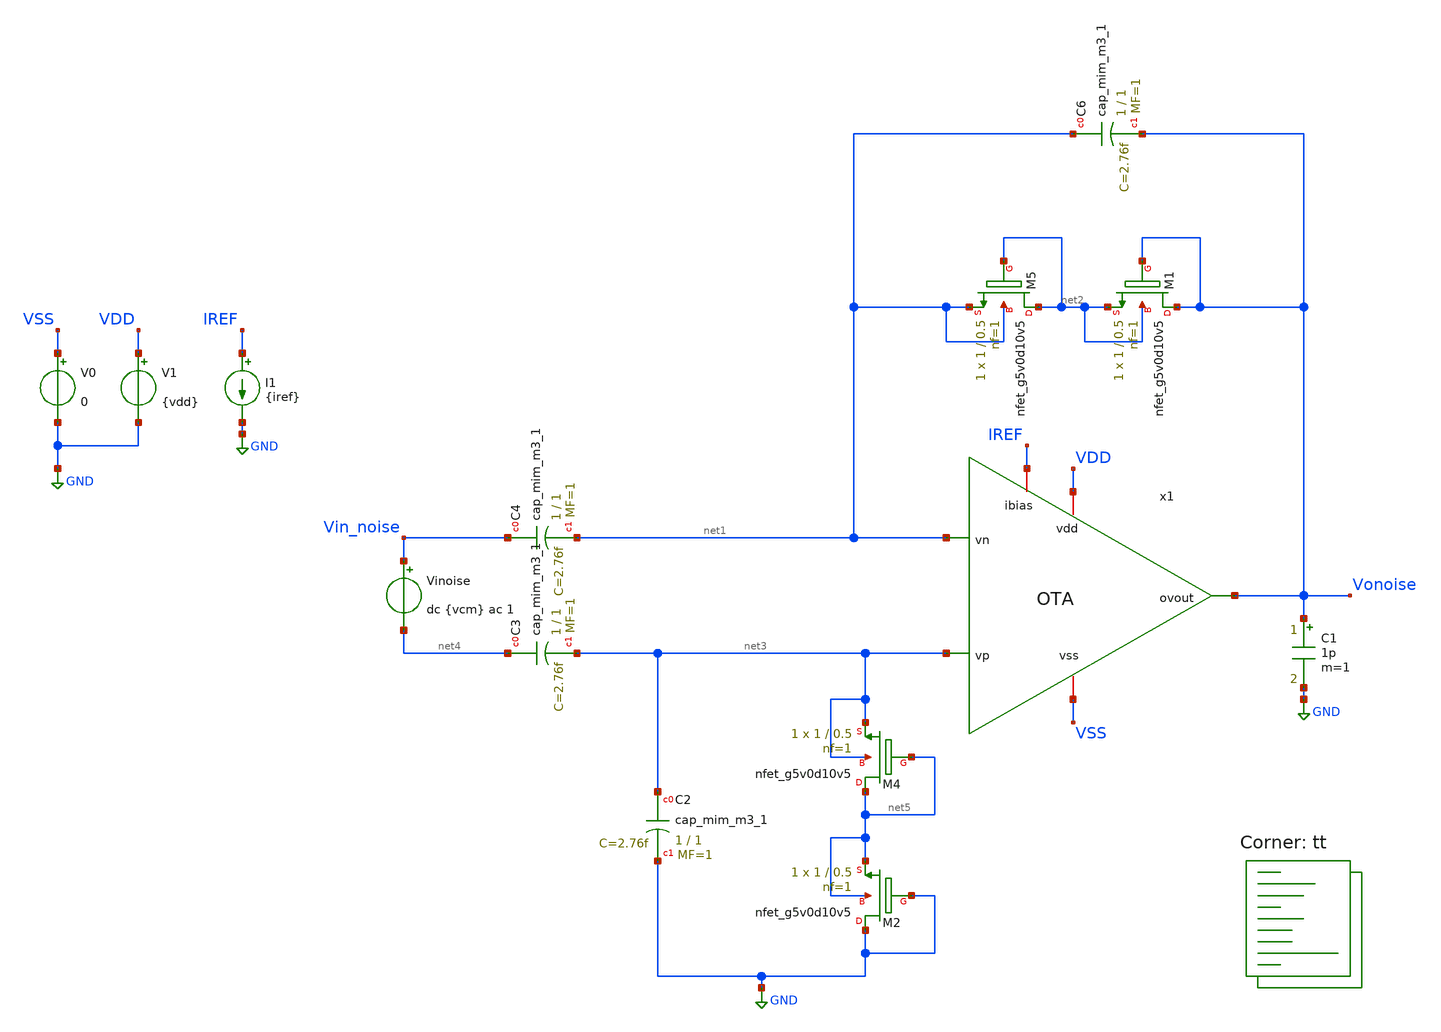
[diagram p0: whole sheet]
** sch_path: xschem/LNA_tb_noise.sch
**.subckt LNA_tb_noise
V0 VSS GND 0
V1 VDD GND {vdd}
C1 Vonoise GND 1p m=1
XC6 net1 Vonoise sky130_fd_pr__cap_mim_m3_1 W=1 L=1 MF=1 m=1
XC2 net3 GND sky130_fd_pr__cap_mim_m3_1 W=1 L=1 MF=1 m=1
XC3 net4 net3 sky130_fd_pr__cap_mim_m3_1 W=1 L=1 MF=1 m=1
XC4 Vin_noise net1 sky130_fd_pr__cap_mim_m3_1 W=1 L=1 MF=1 m=1
XM5 net2 net2 net1 net1 sky130_fd_pr__nfet_g5v0d10v5 L=0.5 W=1 nf=1 ad='int((nf+1)/2) * W/nf * 0.29'
+ as='int((nf+2)/2) * W/nf * 0.29' pd='2*int((nf+1)/2) * (W/nf + 0.29)' ps='2*int((nf+2)/2) * (W/nf + 0.29)'
+ nrd='0.29 / W' nrs='0.29 / W' sa=0 sb=0 sd=0 mult=1 m=1
XM1 Vonoise Vonoise net2 net2 sky130_fd_pr__nfet_g5v0d10v5 L=0.5 W=1 nf=1 ad='int((nf+1)/2) * W/nf * 0.29'
+ as='int((nf+2)/2) * W/nf * 0.29' pd='2*int((nf+1)/2) * (W/nf + 0.29)' ps='2*int((nf+2)/2) * (W/nf + 0.29)'
+ nrd='0.29 / W' nrs='0.29 / W' sa=0 sb=0 sd=0 mult=1 m=1
XM4 net5 net5 net3 net3 sky130_fd_pr__nfet_g5v0d10v5 L=0.5 W=1 nf=1 ad='int((nf+1)/2) * W/nf * 0.29'
+ as='int((nf+2)/2) * W/nf * 0.29' pd='2*int((nf+1)/2) * (W/nf + 0.29)' ps='2*int((nf+2)/2) * (W/nf + 0.29)'
+ nrd='0.29 / W' nrs='0.29 / W' sa=0 sb=0 sd=0 mult=1 m=1
XM2 GND GND net5 net5 sky130_fd_pr__nfet_g5v0d10v5 L=0.5 W=1 nf=1 ad='int((nf+1)/2) * W/nf * 0.29' as='int((nf+2)/2) * W/nf * 0.29'
+ pd='2*int((nf+1)/2) * (W/nf + 0.29)' ps='2*int((nf+2)/2) * (W/nf + 0.29)' nrd='0.29 / W' nrs='0.29 / W'
+ sa=0 sb=0 sd=0 mult=1 m=1
Vinoise Vin_noise net4 dc {vcm} ac 1
I1 IREF GND {iref}
x1 Vonoise VDD VSS IREF net1 net3 OTA
**** begin user architecture code

.param vdd=5
.param vcm=2.5
.param iref = 1u

.control
	save all
	save @m.x1.xm1a.msky130_fd_pr__pfet_g5v0d10v5[id] @m.x1.xm1a.msky130_fd_pr__pfet_g5v0d10v5[gm]
+ @m.x1.xm1a.msky130_fd_pr__pfet_g5v0d10v5[gds]
	save @m.x1.xm1b.msky130_fd_pr__pfet_g5v0d10v5[id] @m.x1.xm1b.msky130_fd_pr__pfet_g5v0d10v5[gm]
+ @m.x1.xm1b.msky130_fd_pr__pfet_g5v0d10v5[gds]
	save @m.x1.xm2a.msky130_fd_pr__pfet_g5v0d10v5[id] @m.x1.xm2a.msky130_fd_pr__pfet_g5v0d10v5[gm]
+ @m.x1.xm2a.msky130_fd_pr__pfet_g5v0d10v5[gds]
	save @m.x1.xm2b.msky130_fd_pr__pfet_g5v0d10v5[id] @m.x1.xm2b.msky130_fd_pr__pfet_g5v0d10v5[gm]
+ @m.x1.xm2b.msky130_fd_pr__pfet_g5v0d10v5[gds]
	save @m.x1.xm3a.msky130_fd_pr__nfet_g5v0d10v5[id] @m.x1.xm3a.msky130_fd_pr__nfet_g5v0d10v5[gm]
+ @m.x1.xm3a.msky130_fd_pr__nfet_g5v0d10v5[gds]
	save @m.x1.xm3b.msky130_fd_pr__nfet_g5v0d10v5[id] @m.x1.xm3b.msky130_fd_pr__nfet_g5v0d10v5[gm]
+ @m.x1.xm3b.msky130_fd_pr__nfet_g5v0d10v5[gds]
	save @m.x1.xm4a.msky130_fd_pr__nfet_g5v0d10v5[id] @m.x1.xm4a.msky130_fd_pr__nfet_g5v0d10v5[gm]
+ @m.x1.xm4a.msky130_fd_pr__nfet_g5v0d10v5[gds]
	save @m.x1.xm4b.msky130_fd_pr__nfet_g5v0d10v5[id] @m.x1.xm4b.msky130_fd_pr__nfet_g5v0d10v5[gm]
+ @m.x1.xm4b.msky130_fd_pr__nfet_g5v0d10v5[gds]
	save @m.x1.xm4c.msky130_fd_pr__nfet_g5v0d10v5[id] @m.x1.xm4c.msky130_fd_pr__nfet_g5v0d10v5[gm]
+ @m.x1.xm4c.msky130_fd_pr__nfet_g5v0d10v5[gds]
	save @m.x1.xm4d.msky130_fd_pr__nfet_g5v0d10v5[id] @m.x1.xm4d.msky130_fd_pr__nfet_g5v0d10v5[gm]
+ @m.x1.xm4d.msky130_fd_pr__nfet_g5v0d10v5[gds]
	save @m.x1.xm5a.msky130_fd_pr__pfet_g5v0d10v5[id] @m.x1.xm5a.msky130_fd_pr__pfet_g5v0d10v5[gm]
+ @m.x1.xm5a.msky130_fd_pr__pfet_g5v0d10v5[gds]
	save @m.x1.xm5b.msky130_fd_pr__pfet_g5v0d10v5[id] @m.x1.xm5b.msky130_fd_pr__pfet_g5v0d10v5[gm]
+ @m.x1.xm5b.msky130_fd_pr__pfet_g5v0d10v5[gds]
	save @m.x1.xm6.msky130_fd_pr__pfet_g5v0d10v5[id] @m.x1.xm6.msky130_fd_pr__pfet_g5v0d10v5[gm]
+ @m.x1.xm6.msky130_fd_pr__pfet_g5v0d10v5[gds]
	save @m.x1.xm7.msky130_fd_pr__pfet_g5v0d10v5[id] @m.x1.xm7.msky130_fd_pr__pfet_g5v0d10v5[gm]
+ @m.x1.xm7.msky130_fd_pr__pfet_g5v0d10v5[gds]

	op
	show

	noise v(Vonoise) Vinoise dec 20 1k 10e9
	setplot noise1
	write LNA_tb_noise1.raw noise1.all
	setplot noise2
	print onoise_total
	write LNA_tb_noise2.raw noise2.all


.endc



.lib $::SKYWATER_MODELS/sky130.lib.spice tt
**** end user architecture code
**.ends

* expanding   symbol:  /home/william/projects/sky130_vbl_ip__LNA/xschem/OTA.sym # of pins=6
** sym_path: xschem/OTA.sym
** sch_path: xschem/OTA.sch
.subckt OTA ovout vdd vss ibias vn vp
*.iopin ibias
*.iopin vdd
*.iopin vss
*.ipin vp
*.ipin vn
*.opin ovout
XM5a net2 vp net1 vdd sky130_fd_pr__pfet_g5v0d10v5 L=0.5 W=80 nf=1 ad='int((nf+1)/2) * W/nf * 0.29' as='int((nf+2)/2) * W/nf * 0.29'
+ pd='2*int((nf+1)/2) * (W/nf + 0.29)' ps='2*int((nf+2)/2) * (W/nf + 0.29)' nrd='0.29 / W' nrs='0.29 / W'
+ sa=0 sb=0 sd=0 mult=1 m=1
XM5b net3 vn net1 vdd sky130_fd_pr__pfet_g5v0d10v5 L=0.5 W=80 nf=1 ad='int((nf+1)/2) * W/nf * 0.29' as='int((nf+2)/2) * W/nf * 0.29'
+ pd='2*int((nf+1)/2) * (W/nf + 0.29)' ps='2*int((nf+2)/2) * (W/nf + 0.29)' nrd='0.29 / W' nrs='0.29 / W'
+ sa=0 sb=0 sd=0 mult=1 m=1
XM4b net2 net2 vss vss sky130_fd_pr__nfet_g5v0d10v5 L=4 W=1 nf=1 ad='int((nf+1)/2) * W/nf * 0.29' as='int((nf+2)/2) * W/nf * 0.29'
+ pd='2*int((nf+1)/2) * (W/nf + 0.29)' ps='2*int((nf+2)/2) * (W/nf + 0.29)' nrd='0.29 / W' nrs='0.29 / W'
+ sa=0 sb=0 sd=0 mult=1 m=1
XM4c net3 net3 vss vss sky130_fd_pr__nfet_g5v0d10v5 L=4 W=1 nf=1 ad='int((nf+1)/2) * W/nf * 0.29' as='int((nf+2)/2) * W/nf * 0.29'
+ pd='2*int((nf+1)/2) * (W/nf + 0.29)' ps='2*int((nf+2)/2) * (W/nf + 0.29)' nrd='0.29 / W' nrs='0.29 / W'
+ sa=0 sb=0 sd=0 mult=1 m=1
XM4a net5 net2 vss vss sky130_fd_pr__nfet_g5v0d10v5 L=4 W=1 nf=1 ad='int((nf+1)/2) * W/nf * 0.29' as='int((nf+2)/2) * W/nf * 0.29'
+ pd='2*int((nf+1)/2) * (W/nf + 0.29)' ps='2*int((nf+2)/2) * (W/nf + 0.29)' nrd='0.29 / W' nrs='0.29 / W'
+ sa=0 sb=0 sd=0 mult=1 m=1
XM4d net7 net3 vss vss sky130_fd_pr__nfet_g5v0d10v5 L=4 W=1 nf=1 ad='int((nf+1)/2) * W/nf * 0.29' as='int((nf+2)/2) * W/nf * 0.29'
+ pd='2*int((nf+1)/2) * (W/nf + 0.29)' ps='2*int((nf+2)/2) * (W/nf + 0.29)' nrd='0.29 / W' nrs='0.29 / W'
+ sa=0 sb=0 sd=0 mult=1 m=1
XM1a net4 net4 vdd vdd sky130_fd_pr__pfet_g5v0d10v5 L=1 W=0.6 nf=1 ad='int((nf+1)/2) * W/nf * 0.29' as='int((nf+2)/2) * W/nf * 0.29'
+ pd='2*int((nf+1)/2) * (W/nf + 0.29)' ps='2*int((nf+2)/2) * (W/nf + 0.29)' nrd='0.29 / W' nrs='0.29 / W'
+ sa=0 sb=0 sd=0 mult=1 m=1
XM1b net8 net4 vdd vdd sky130_fd_pr__pfet_g5v0d10v5 L=1 W=0.6 nf=1 ad='int((nf+1)/2) * W/nf * 0.29' as='int((nf+2)/2) * W/nf * 0.29'
+ pd='2*int((nf+1)/2) * (W/nf + 0.29)' ps='2*int((nf+2)/2) * (W/nf + 0.29)' nrd='0.29 / W' nrs='0.29 / W'
+ sa=0 sb=0 sd=0 mult=1 m=1
XM7 ibias ibias vdd vdd sky130_fd_pr__pfet_g5v0d10v5 L=2 W=2 nf=1 ad='int((nf+1)/2) * W/nf * 0.29' as='int((nf+2)/2) * W/nf * 0.29'
+ pd='2*int((nf+1)/2) * (W/nf + 0.29)' ps='2*int((nf+2)/2) * (W/nf + 0.29)' nrd='0.29 / W' nrs='0.29 / W'
+ sa=0 sb=0 sd=0 mult=1 m=1
XM6 net1 ibias vdd vdd sky130_fd_pr__pfet_g5v0d10v5 L=2 W=2 nf=1 ad='int((nf+1)/2) * W/nf * 0.29' as='int((nf+2)/2) * W/nf * 0.29'
+ pd='2*int((nf+1)/2) * (W/nf + 0.29)' ps='2*int((nf+2)/2) * (W/nf + 0.29)' nrd='0.29 / W' nrs='0.29 / W'
+ sa=0 sb=0 sd=0 mult=1 m=1
XM3a net6 net6 net5 vss sky130_fd_pr__nfet_g5v0d10v5 L=4 W=1 nf=1 ad='int((nf+1)/2) * W/nf * 0.29' as='int((nf+2)/2) * W/nf * 0.29'
+ pd='2*int((nf+1)/2) * (W/nf + 0.29)' ps='2*int((nf+2)/2) * (W/nf + 0.29)' nrd='0.29 / W' nrs='0.29 / W'
+ sa=0 sb=0 sd=0 mult=1 m=1
XM2a net6 net6 net4 vdd sky130_fd_pr__pfet_g5v0d10v5 L=1 W=0.6 nf=1 ad='int((nf+1)/2) * W/nf * 0.29'
+ as='int((nf+2)/2) * W/nf * 0.29' pd='2*int((nf+1)/2) * (W/nf + 0.29)' ps='2*int((nf+2)/2) * (W/nf + 0.29)'
+ nrd='0.29 / W' nrs='0.29 / W' sa=0 sb=0 sd=0 mult=1 m=1
XM2b ovout ovout net8 vdd sky130_fd_pr__pfet_g5v0d10v5 L=1 W=0.6 nf=1 ad='int((nf+1)/2) * W/nf * 0.29'
+ as='int((nf+2)/2) * W/nf * 0.29' pd='2*int((nf+1)/2) * (W/nf + 0.29)' ps='2*int((nf+2)/2) * (W/nf + 0.29)'
+ nrd='0.29 / W' nrs='0.29 / W' sa=0 sb=0 sd=0 mult=1 m=1
XM3b ovout ovout net7 vss sky130_fd_pr__nfet_g5v0d10v5 L=4 W=1 nf=1 ad='int((nf+1)/2) * W/nf * 0.29'
+ as='int((nf+2)/2) * W/nf * 0.29' pd='2*int((nf+1)/2) * (W/nf + 0.29)' ps='2*int((nf+2)/2) * (W/nf + 0.29)'
+ nrd='0.29 / W' nrs='0.29 / W' sa=0 sb=0 sd=0 mult=1 m=1
.ends

.GLOBAL GND
.end
